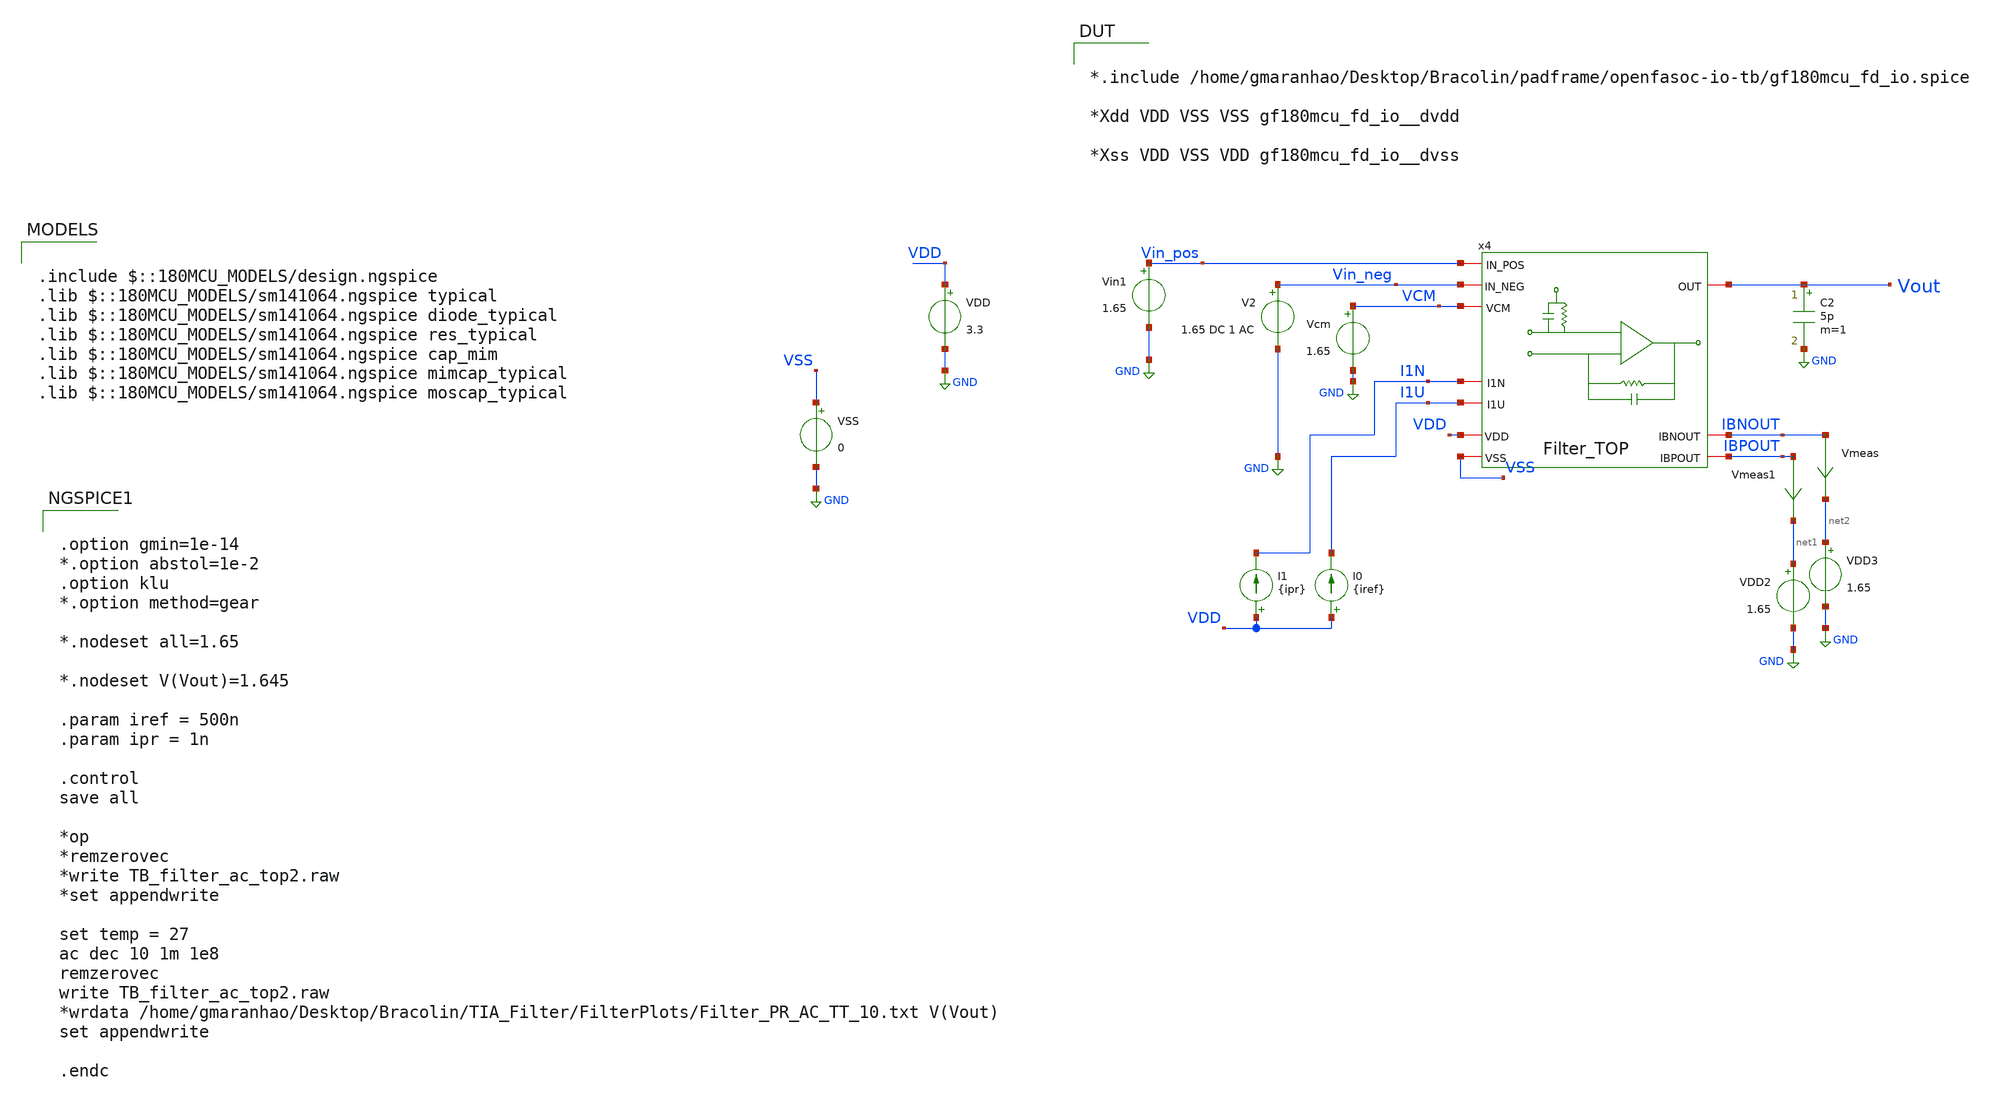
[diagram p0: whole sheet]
** sch_path: TIA_Filter/TB_filter_ac_top2.sch
**.subckt TB_filter_ac_top2
VDD VDD GND 3.3
C2 Vout GND 5p m=1
Vin1 Vin_pos GND 1.65
V2 Vin_neg GND 1.65 DC 1 AC
I0 VDD I1U {iref}
I1 VDD I1N {ipr}
Vmeas IBNOUT net2 0
.save i(vmeas)
Vmeas1 IBPOUT net1 0
.save i(vmeas1)
Vcm VCM GND 1.65
VDD2 net1 GND 1.65
VDD3 net2 GND 1.65
x4 Vin_pos Vin_neg VCM Vout VDD VSS I1N I1U IBNOUT IBPOUT Filter_TOP
VSS VSS GND 0
**** begin user architecture code


.option gmin=1e-14
*.option abstol=1e-2
.option klu
*.option method=gear

*.nodeset all=1.65

*.nodeset V(Vout)=1.645

.param iref = 500n
.param ipr = 1n

.control
save all

*op
*remzerovec
*write TB_filter_ac_top2.raw
*set appendwrite

set temp = 27
ac dec 10 1m 1e8
remzerovec
write TB_filter_ac_top2.raw
*wrdata /home/gmaranhao/Desktop/Bracolin/TIA_Filter/FilterPlots/Filter_PR_AC_TT_10.txt V(Vout)
set appendwrite

.endc



*.include /home/gmaranhao/Desktop/Bracolin/padframe/openfasoc-io-tb/gf180mcu_fd_io.spice

*Xdd VDD VSS VSS gf180mcu_fd_io__dvdd

*Xss VDD VSS VDD gf180mcu_fd_io__dvss


.include $::180MCU_MODELS/design.ngspice
.lib $::180MCU_MODELS/sm141064.ngspice typical
.lib $::180MCU_MODELS/sm141064.ngspice diode_typical
.lib $::180MCU_MODELS/sm141064.ngspice res_typical
.lib $::180MCU_MODELS/sm141064.ngspice cap_mim
.lib $::180MCU_MODELS/sm141064.ngspice mimcap_typical
.lib $::180MCU_MODELS/sm141064.ngspice moscap_typical

**** end user architecture code
**.ends
.GLOBAL GND
.end
